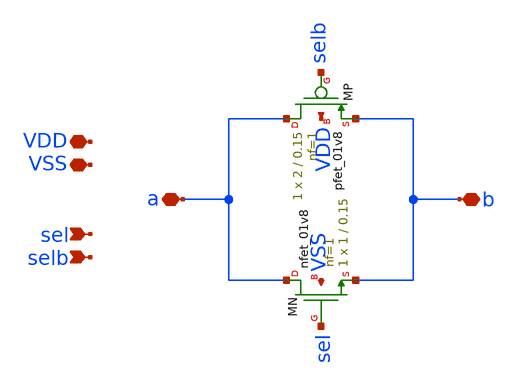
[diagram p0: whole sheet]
** sch_path: xsch/ip/tgate/tgate_2t.sch
**.subckt tgate_2t a b VDD VSS sel selb
*.iopin a
*.iopin b
*.iopin VDD
*.iopin VSS
*.ipin sel
*.ipin selb
XMP a selb b VDD sky130_fd_pr__pfet_01v8 L=0.15 W=2 nf=1 ad='int((nf+1)/2) * W/nf * 0.29' as='int((nf+2)/2) * W/nf * 0.29'
+ pd='2*int((nf+1)/2) * (W/nf + 0.29)' ps='2*int((nf+2)/2) * (W/nf + 0.29)' nrd='0.29 / W' nrs='0.29 / W'
+ sa=0 sb=0 sd=0 mult=1 m=1
XMN a sel b VSS sky130_fd_pr__nfet_01v8 L=0.15 W=1 nf=1 ad='int((1 + 1)/2) * 1 / 1 * 0.29' as='int((1 + 2)/2) * 1 / 1 * 0.29'
+ pd='2*int((1 + 1)/2) * (1 / 1 + 0.29)' ps='2*int((1 + 2)/2) * (1 / 1 + 0.29)' nrd='0.29 / 1 ' nrs='0.29 / 1 '
+ sa=0 sb=0 sd=0 mult=1 m=1
**.ends
.end
